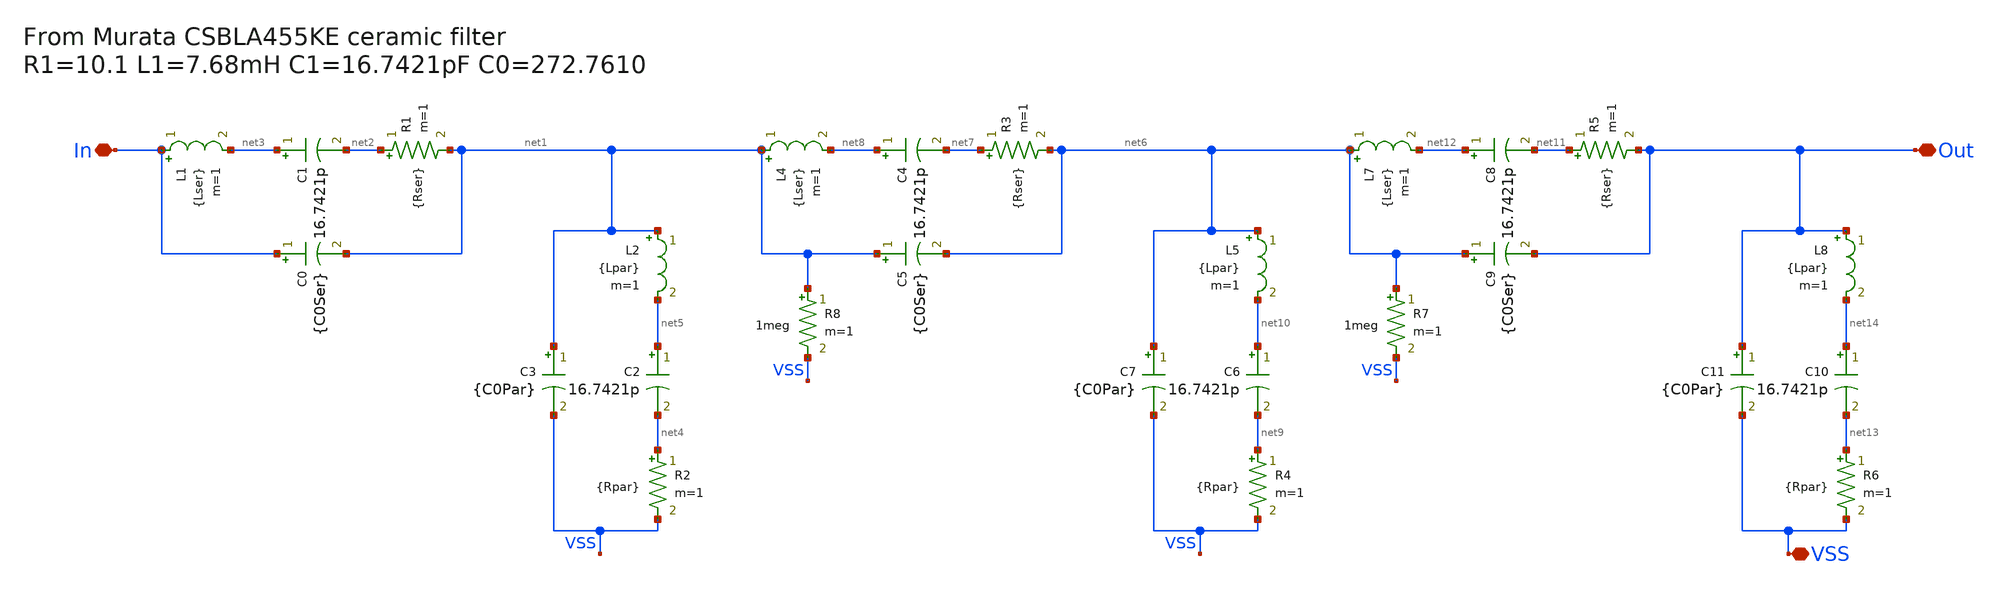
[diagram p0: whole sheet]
** sch_path: Project/mag/455_crystal.sch
**.subckt 455_crystal Out In VSS
*.iopin Out
*.iopin In
*.iopin VSS
R1 net2 net1 {Rser} m=1
L1 In net3 {Lser} m=1
C1 net3 net2 16.7421p m=1
C0 In net1 {C0Ser} m=1
R2 net4 VSS {Rpar} m=1
L2 net1 net5 {Lpar} m=1
C2 net5 net4 16.7421p m=1
C3 net1 VSS {C0Par} m=1
R3 net7 net6 {Rser} m=1
L4 net1 net8 {Lser} m=1
C4 net8 net7 16.7421p m=1
C5 net1 net6 {C0Ser} m=1
R4 net9 VSS {Rpar} m=1
L5 net6 net10 {Lpar} m=1
C6 net10 net9 16.7421p m=1
C7 net6 VSS {C0Par} m=1
R5 net11 Out {Rser} m=1
L7 net6 net12 {Lser} m=1
C8 net12 net11 16.7421p m=1
C9 net6 Out {C0Ser} m=1
R6 net13 VSS {Rpar} m=1
L8 Out net14 {Lpar} m=1
C10 net14 net13 16.7421p m=1
C11 Out VSS {C0Par} m=1
R7 net6 VSS 1meg m=1
R8 net1 VSS 1meg m=1
**** begin user architecture code



* ngspice commands
.param Rser=250 Rpar=250 Lser=7.45m Lpar=7.55m C0Ser=272.761p C0par=272.761p



**** end user architecture code
**.ends
.end
